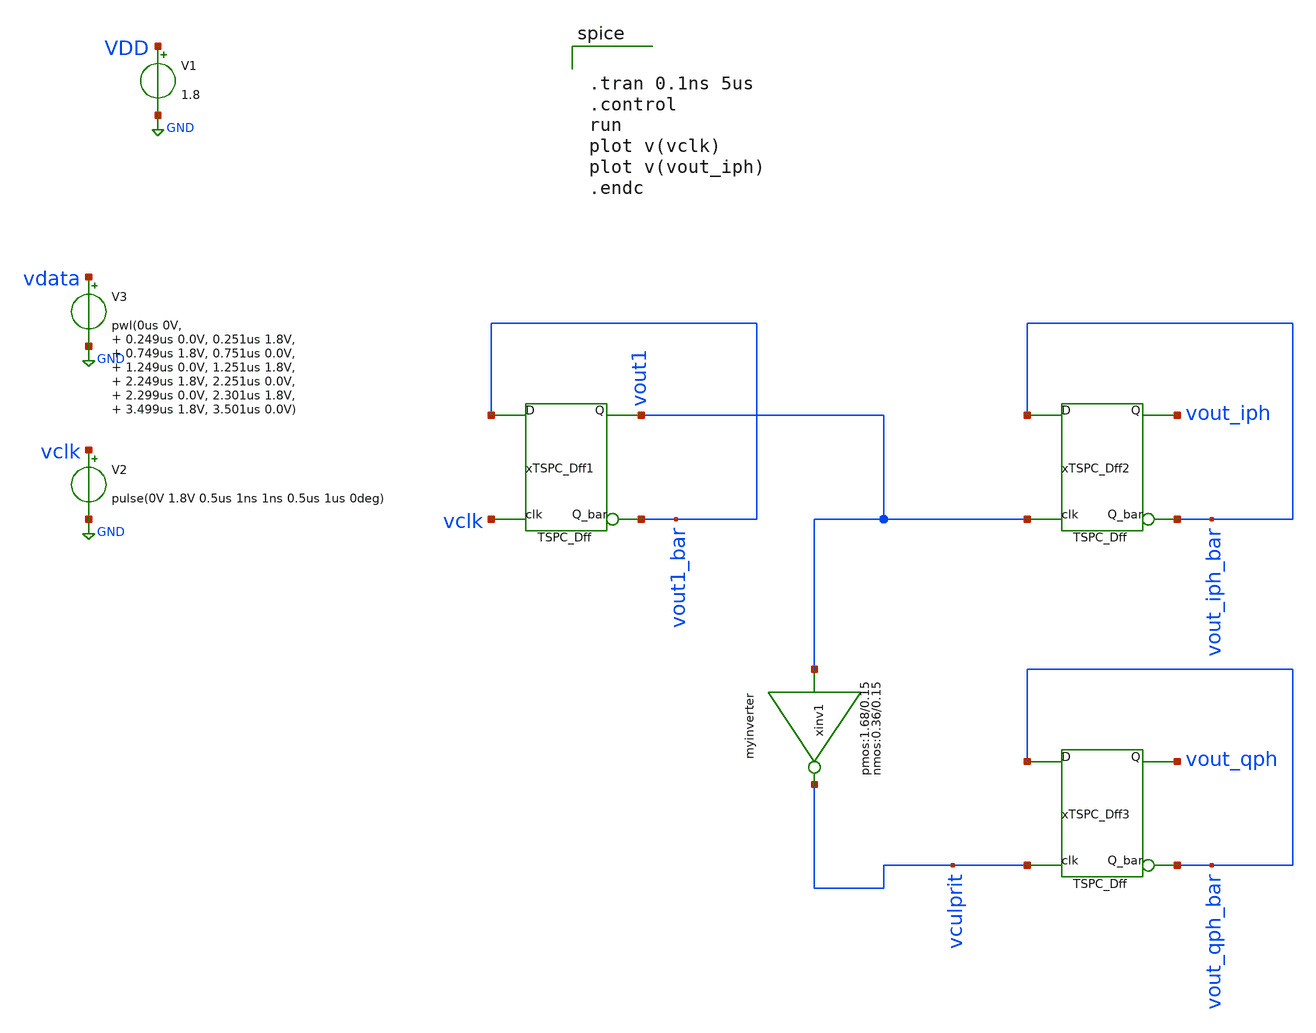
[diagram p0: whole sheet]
** sch_path: testingTSPC_Dff.sch
**.subckt testingTSPC_Dff
V1 VDD GND 1.8
V2 vclk GND pulse(0V 1.8V 0.5us 1ns 1ns 0.5us 1us 0deg)
V3 vdata GND pwl(0us 0V, 0.249us 0.0V, 0.251us 1.8V, 0.749us 1.8V, 0.751us 0.0V, 1.249us 0.0V,
+ 1.251us 1.8V, 2.249us 1.8V, 2.251us 0.0V, 2.299us 0.0V, 2.301us 1.8V, 3.499us 1.8V, 3.501us 0.0V)
xTSPC_Dff1 vclk vout1_bar vout1_bar vout1 TSPC_Dff
xTSPC_Dff2 vout1 vout_iph_bar vout_iph_bar vout_iph TSPC_Dff
xTSPC_Dff3 vculprit vout_qph_bar vout_qph_bar vout_qph TSPC_Dff
xinv1 vout1 vculprit VDD VSS myinverter wnmos=0.36 lnmos=0.15 wpmos=1.68 lpmos=0.15 m=1
**** begin user architecture code


.tran 0.1ns 5us
.control
run
plot v(vclk)
plot v(vout_iph)
.endc



*.lib ~/open_pdks/sky130/sky130A/libs.tech/ngspice/sky130.lib.spice tt
.param mc_mm_switch=0
.param mc_pr_switch=0

.include ~/open_pdks/sky130/sky130A/libs.tech/ngspice/corners/tt/nonfet.spice


*model
.include ~/open_pdks/sky130/sky130A/libs.tech/ngspice/all.spice

*mosfet
.include ~/open_pdks/sky130/sky130A/libs.ref/sky130_fd_pr/spice/sky130_fd_pr__pfet_01v8__tt.corner.spice
.inclued ~/open_pdks/sky130/sky130A/libs.ref/sky130_fd_pr/spice/sky130_fd_pr__nfet_01v8__tt.corner.spice

*mismatch parameters
.include ~/open_pdks/sky130/sky130A/libs.ref/sky130_fd_pr/spice/sky130_fd_pr__pfet_01v8__mismatch.corner.spice
.include ~/open_pdks/sky130/sky130A/libs.ref/sky130_fd_pr/spice/sky130_fd_pr__nfet_01v8__mismatch.corner.spice

**** end user architecture code
**.ends
.GLOBAL GND
.end
